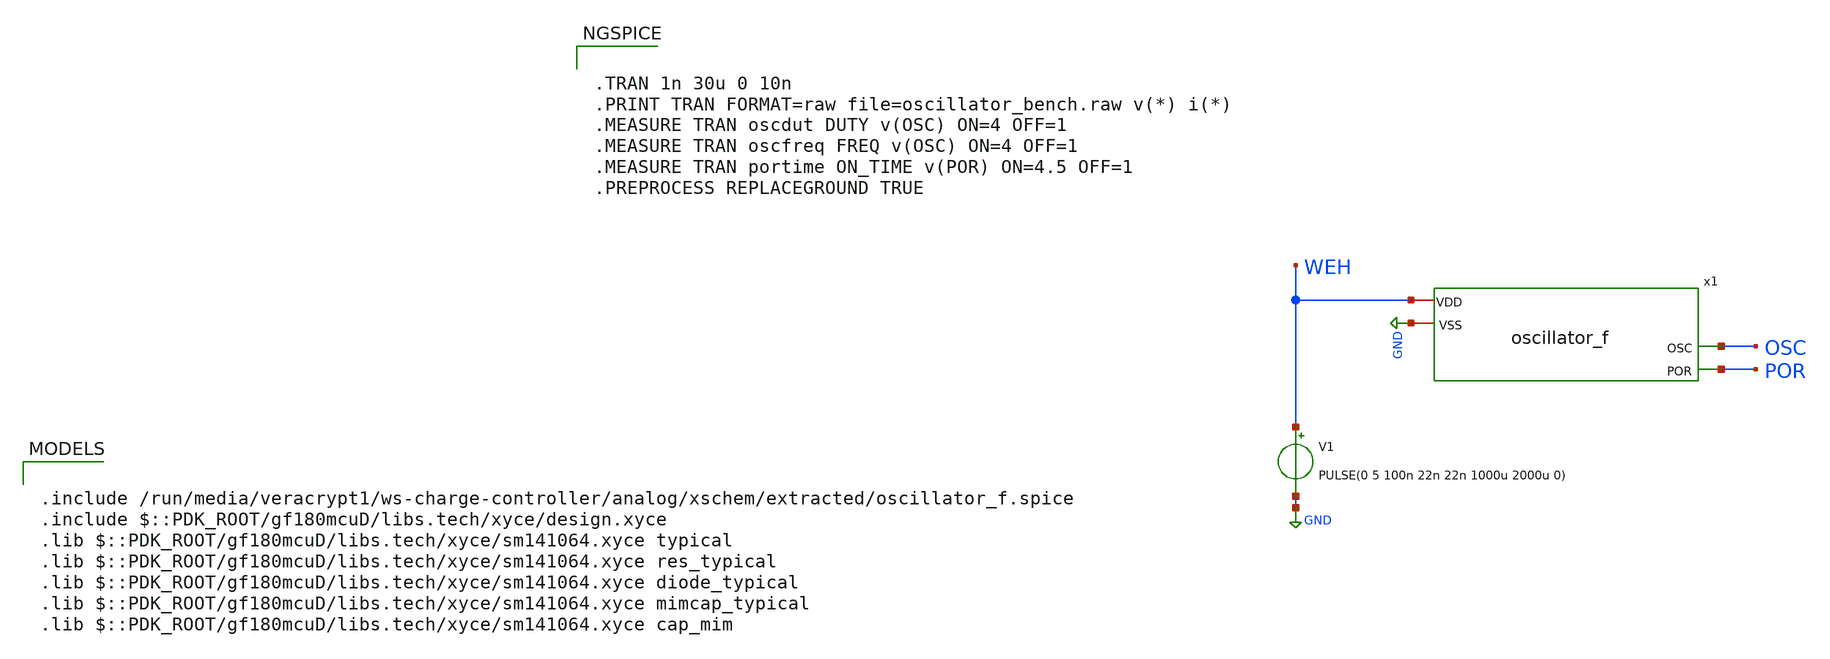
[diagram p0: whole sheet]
** sch_path: analog/xschem/oscillator_bench.sch
**.subckt oscillator_bench
V1 WEH GND PULSE(0 5 100n 22n 22n 1000u 2000u 0)
x1 WEH GND OSC POR oscillator_f
**** begin user architecture code


.TRAN 1n 30u 0 10n
.PRINT TRAN FORMAT=raw file=oscillator_bench.raw v(*) i(*)
.MEASURE TRAN oscdut DUTY v(OSC) ON=4 OFF=1
.MEASURE TRAN oscfreq FREQ v(OSC) ON=4 OFF=1
.MEASURE TRAN portime ON_TIME v(POR) ON=4.5 OFF=1
.PREPROCESS REPLACEGROUND TRUE



.include /run/media/veracrypt1/ws-charge-controller/analog/xschem/extracted/oscillator_f.spice
.include $::PDK_ROOT/gf180mcuD/libs.tech/xyce/design.xyce
.lib $::PDK_ROOT/gf180mcuD/libs.tech/xyce/sm141064.xyce typical
.lib $::PDK_ROOT/gf180mcuD/libs.tech/xyce/sm141064.xyce res_typical
.lib $::PDK_ROOT/gf180mcuD/libs.tech/xyce/sm141064.xyce diode_typical
.lib $::PDK_ROOT/gf180mcuD/libs.tech/xyce/sm141064.xyce mimcap_typical
.lib $::PDK_ROOT/gf180mcuD/libs.tech/xyce/sm141064.xyce cap_mim

**** end user architecture code
**.ends
.GLOBAL GND
.end
